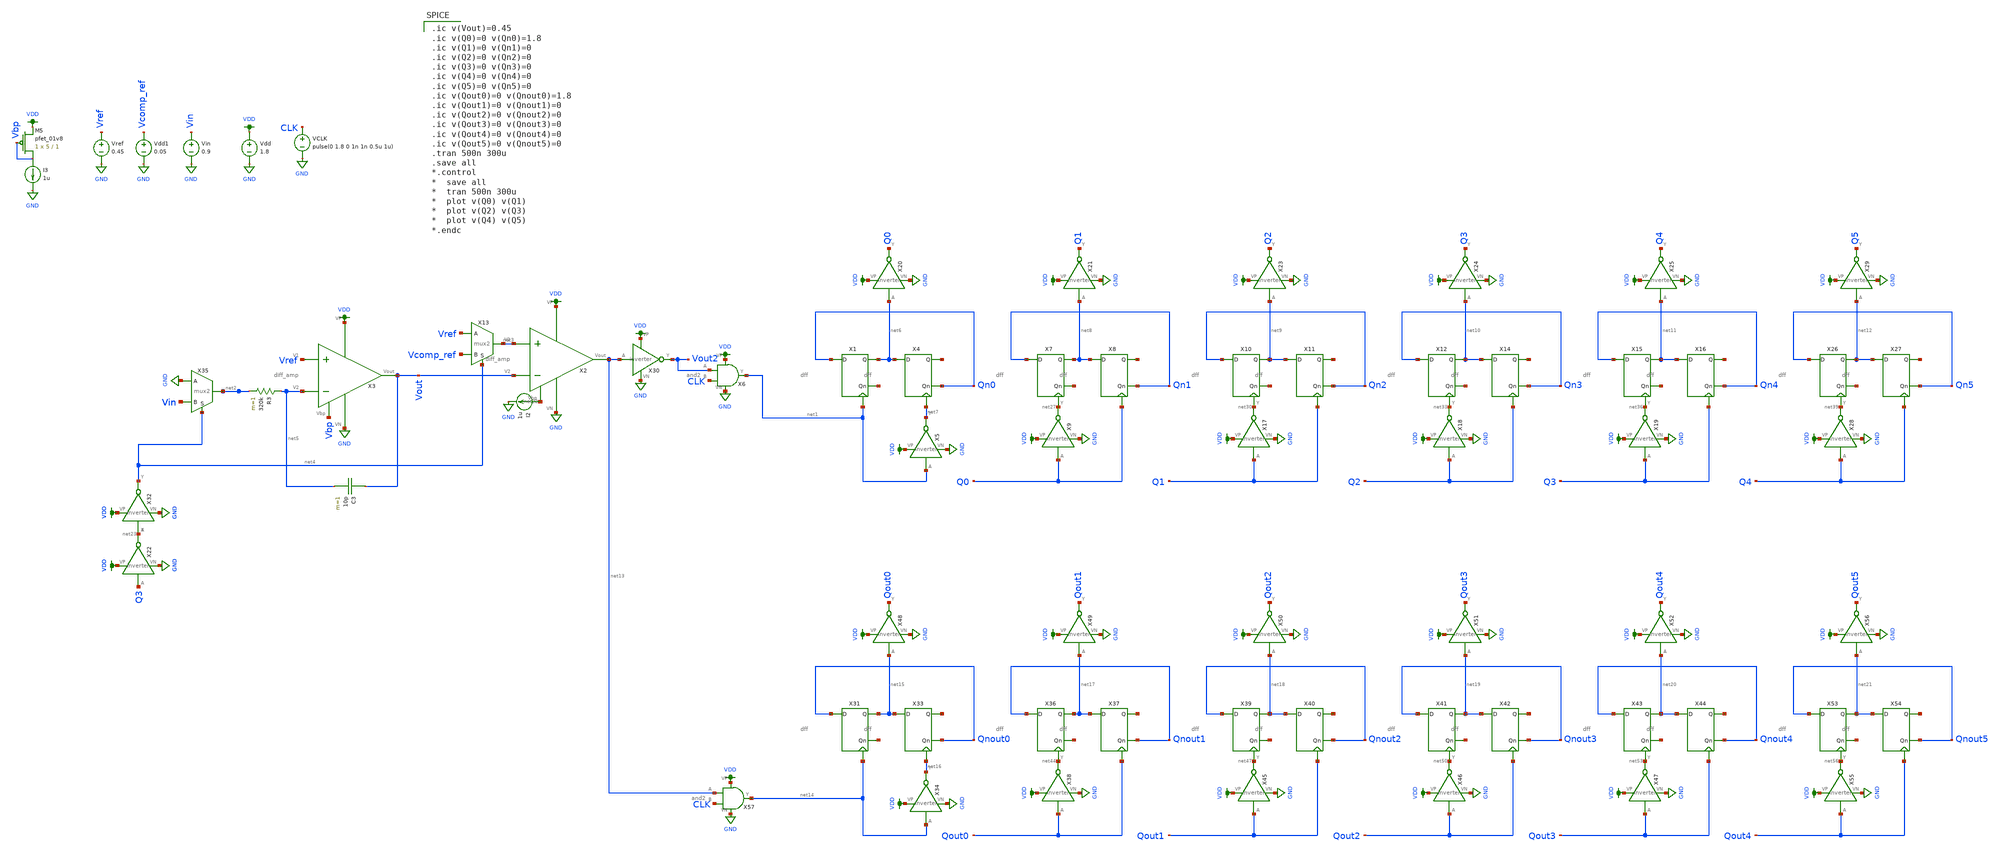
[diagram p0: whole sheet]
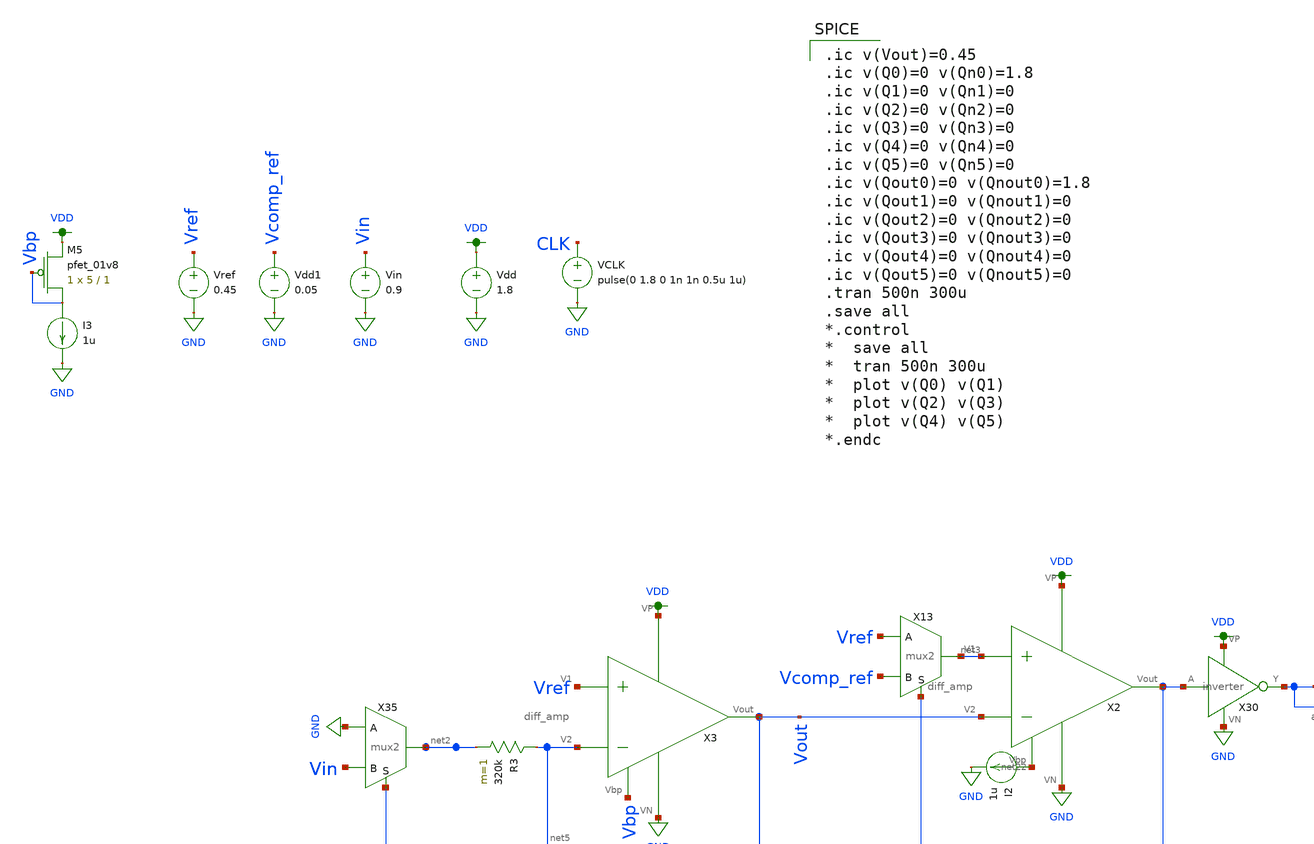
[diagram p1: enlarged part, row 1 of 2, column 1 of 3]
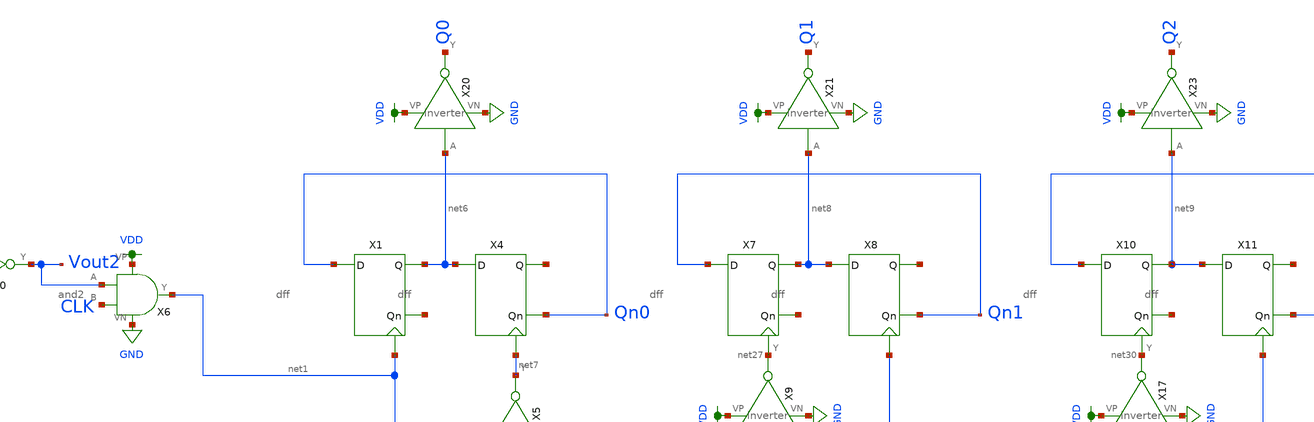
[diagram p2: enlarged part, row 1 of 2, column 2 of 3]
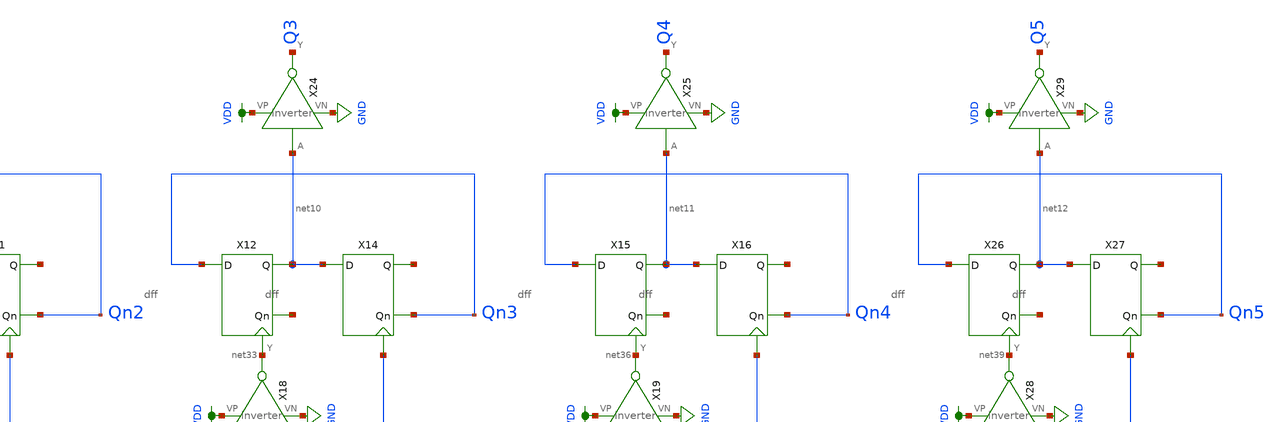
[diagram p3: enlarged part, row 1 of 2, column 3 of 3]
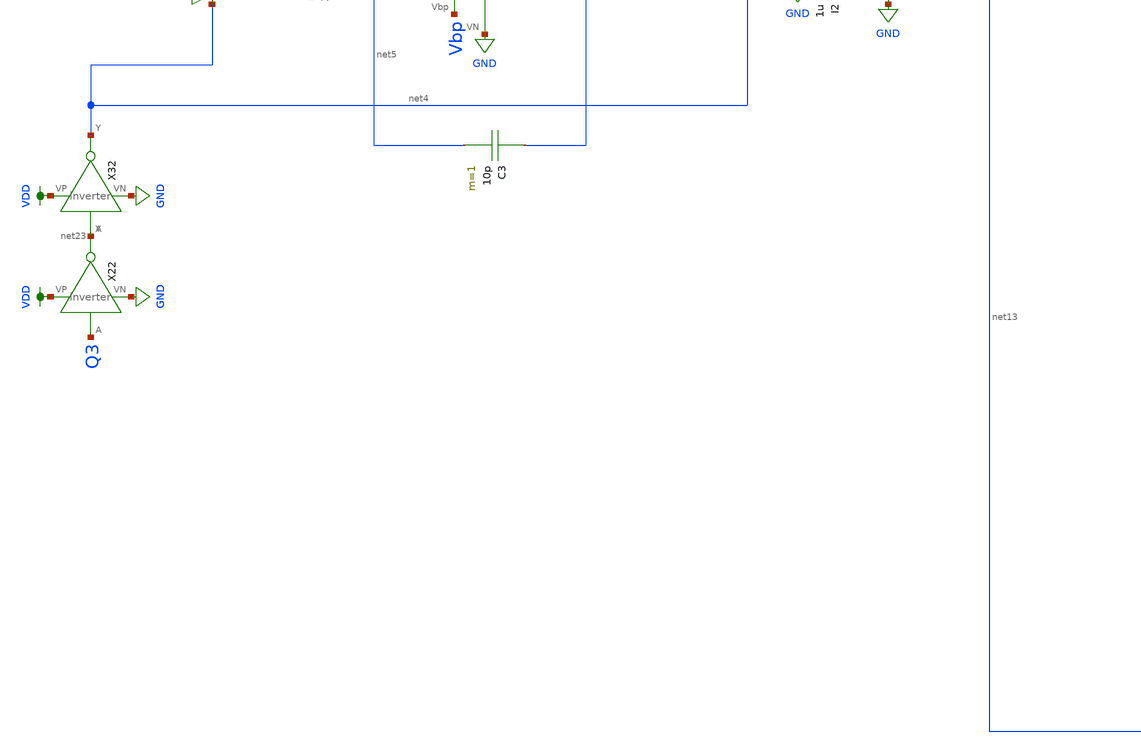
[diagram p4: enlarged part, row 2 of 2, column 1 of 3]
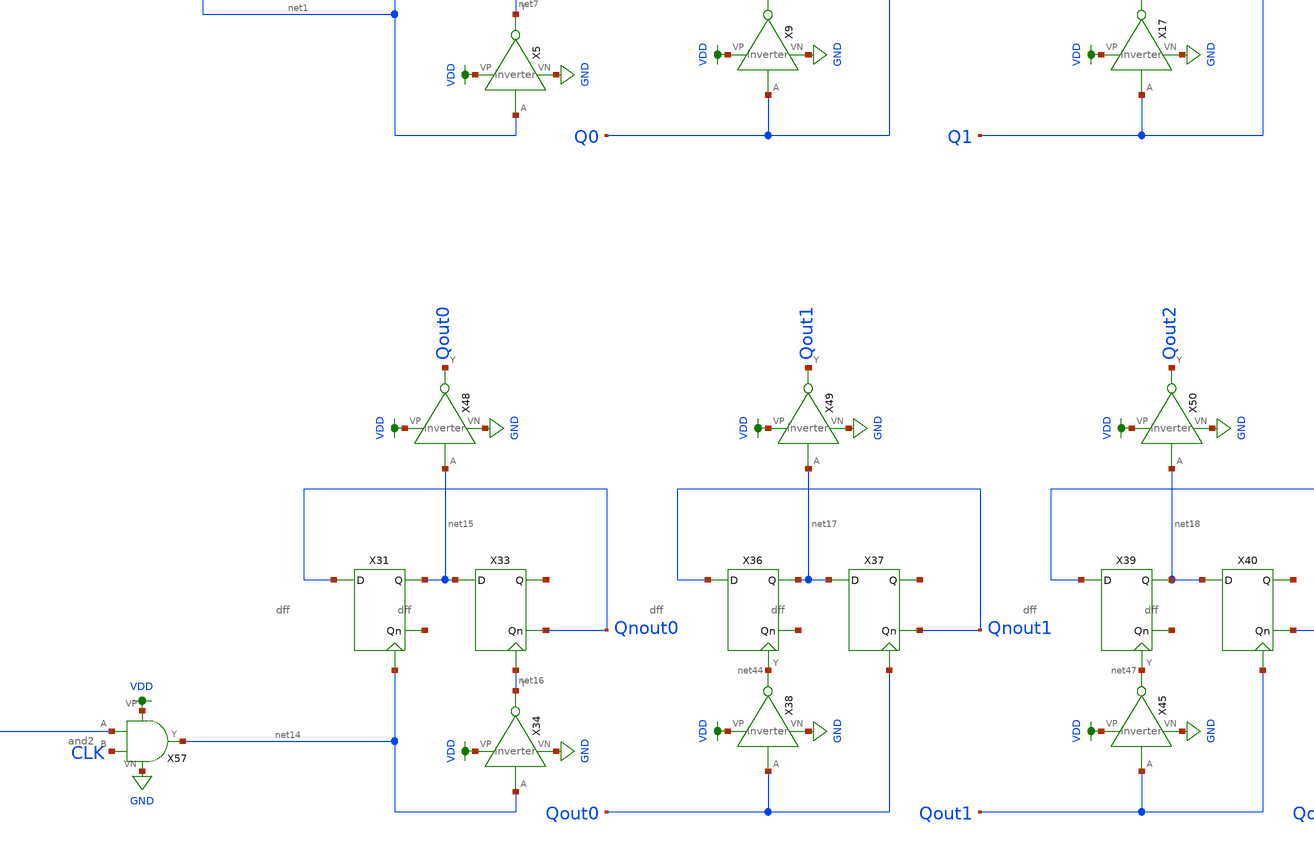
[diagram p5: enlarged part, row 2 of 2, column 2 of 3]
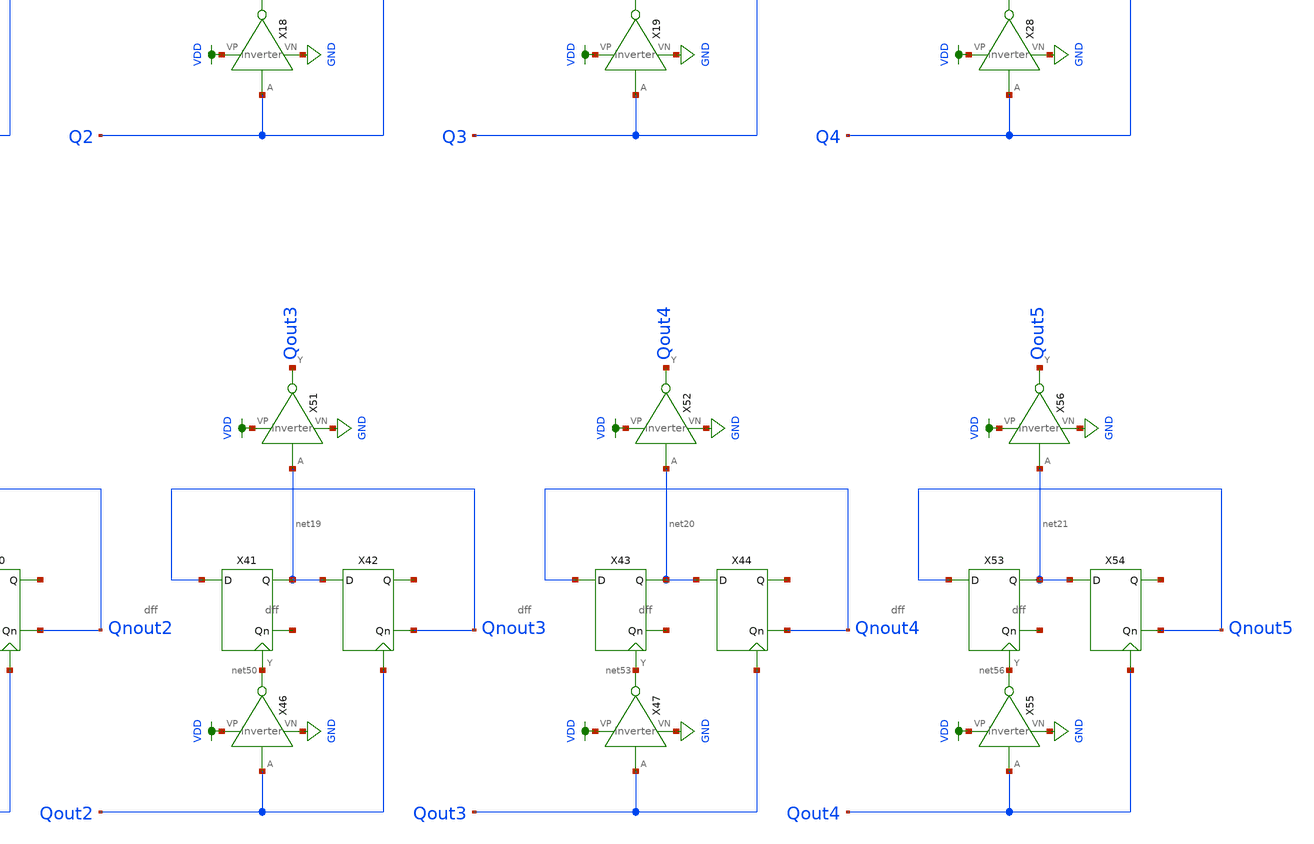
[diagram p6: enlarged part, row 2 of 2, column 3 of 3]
** sch_path: schematic/double-slope-works.sch
**.subckt double-slope-works
X2 VDD net22 net13 net3 Vout GND diff_amp
Vdd VDD GND 1.8
VCLK CLK GND pulse(0 1.8 0 1n 1n 0.5u 1u)
Vdd1 Vcomp_ref GND 0.05
Vin Vin GND 0.9
I2 net22 GND 1u
X6 VDD Vout2 GND net1 CLK and2
X13 net3 Vref Vcomp_ref net4 mux2
X22 Q3 net23 VDD GND inverter
X32 net23 net4 VDD GND inverter
X35 net2 GND Vin net4 mux2
XM5 Vbp Vbp VDD VDD sky130_fd_pr__pfet_01v8 L=1 W=5 nf=1 ad='int((nf+1)/2) * W/nf * 0.29' as='int((nf+2)/2) * W/nf * 0.29'
+ pd='2*int((nf+1)/2) * (W/nf + 0.29)' ps='2*int((nf+2)/2) * (W/nf + 0.29)' nrd='0.29 / W' nrs='0.29 / W'
+ sa=0 sb=0 sd=0 mult=1 m=1
I3 Vbp GND 1u
C3 Vout net5 10p m=1
X3 VDD Vbp Vout Vref net5 GND diff_amp
R3 net5 net2 320k m=1
Vref Vref GND 0.45
X1 Qn0 net24 net6 net1 dff
X4 net6 Qn0 net25 net7 dff
X5 net1 net7 VDD GND inverter
X7 Qn1 net26 net8 net27 dff
X8 net8 Qn1 net28 Q0 dff
X9 Q0 net27 VDD GND inverter
X10 Qn2 net29 net9 net30 dff
X11 net9 Qn2 net31 Q1 dff
X12 Qn3 net32 net10 net33 dff
X14 net10 Qn3 net34 Q2 dff
X15 Qn4 net35 net11 net36 dff
X16 net11 Qn4 net37 Q3 dff
X17 Q1 net30 VDD GND inverter
X18 Q2 net33 VDD GND inverter
X19 Q3 net36 VDD GND inverter
X20 net6 Q0 VDD GND inverter
X21 net8 Q1 VDD GND inverter
X23 net9 Q2 VDD GND inverter
X24 net10 Q3 VDD GND inverter
X25 net11 Q4 VDD GND inverter
X26 Qn5 net38 net12 net39 dff
X27 net12 Qn5 net40 Q4 dff
X28 Q4 net39 VDD GND inverter
X29 net12 Q5 VDD GND inverter
X30 net13 Vout2 VDD GND inverter
X31 Qnout0 net41 net15 net14 dff
X33 net15 Qnout0 net42 net16 dff
X34 net14 net16 VDD GND inverter
X36 Qnout1 net43 net17 net44 dff
X37 net17 Qnout1 net45 Qout0 dff
X38 Qout0 net44 VDD GND inverter
X39 Qnout2 net46 net18 net47 dff
X40 net18 Qnout2 net48 Qout1 dff
X41 Qnout3 net49 net19 net50 dff
X42 net19 Qnout3 net51 Qout2 dff
X43 Qnout4 net52 net20 net53 dff
X44 net20 Qnout4 net54 Qout3 dff
X45 Qout1 net47 VDD GND inverter
X46 Qout2 net50 VDD GND inverter
X47 Qout3 net53 VDD GND inverter
X48 net15 Qout0 VDD GND inverter
X49 net17 Qout1 VDD GND inverter
X50 net18 Qout2 VDD GND inverter
X51 net19 Qout3 VDD GND inverter
X52 net20 Qout4 VDD GND inverter
X53 Qnout5 net55 net21 net56 dff
X54 net21 Qnout5 net57 Qout4 dff
X55 Qout4 net56 VDD GND inverter
X56 net21 Qout5 VDD GND inverter
X57 VDD net13 GND net14 CLK and2
**** begin user architecture code

.ic v(Vout)=0.45
.ic v(Q0)=0 v(Qn0)=1.8
.ic v(Q1)=0 v(Qn1)=0
.ic v(Q2)=0 v(Qn2)=0
.ic v(Q3)=0 v(Qn3)=0
.ic v(Q4)=0 v(Qn4)=0
.ic v(Q5)=0 v(Qn5)=0
.ic v(Qout0)=0 v(Qnout0)=1.8
.ic v(Qout1)=0 v(Qnout1)=0
.ic v(Qout2)=0 v(Qnout2)=0
.ic v(Qout3)=0 v(Qnout3)=0
.ic v(Qout4)=0 v(Qnout4)=0
.ic v(Qout5)=0 v(Qnout5)=0
.tran 500n 300u
.save all
*.control
*  save all
*  tran 500n 300u
*  plot v(Q0) v(Q1)
*  plot v(Q2) v(Q3)
*  plot v(Q4) v(Q5)
*.endc


.option wnflag=1
.param MC_SWITCH=0.0
.lib ~/skywater/skywater-pdk/libraries/sky130_fd_pr_ngspice/latest/models/sky130.lib.spice tt

**** end user architecture code
**.ends
.GLOBAL GND
.GLOBAL VDD
.end
